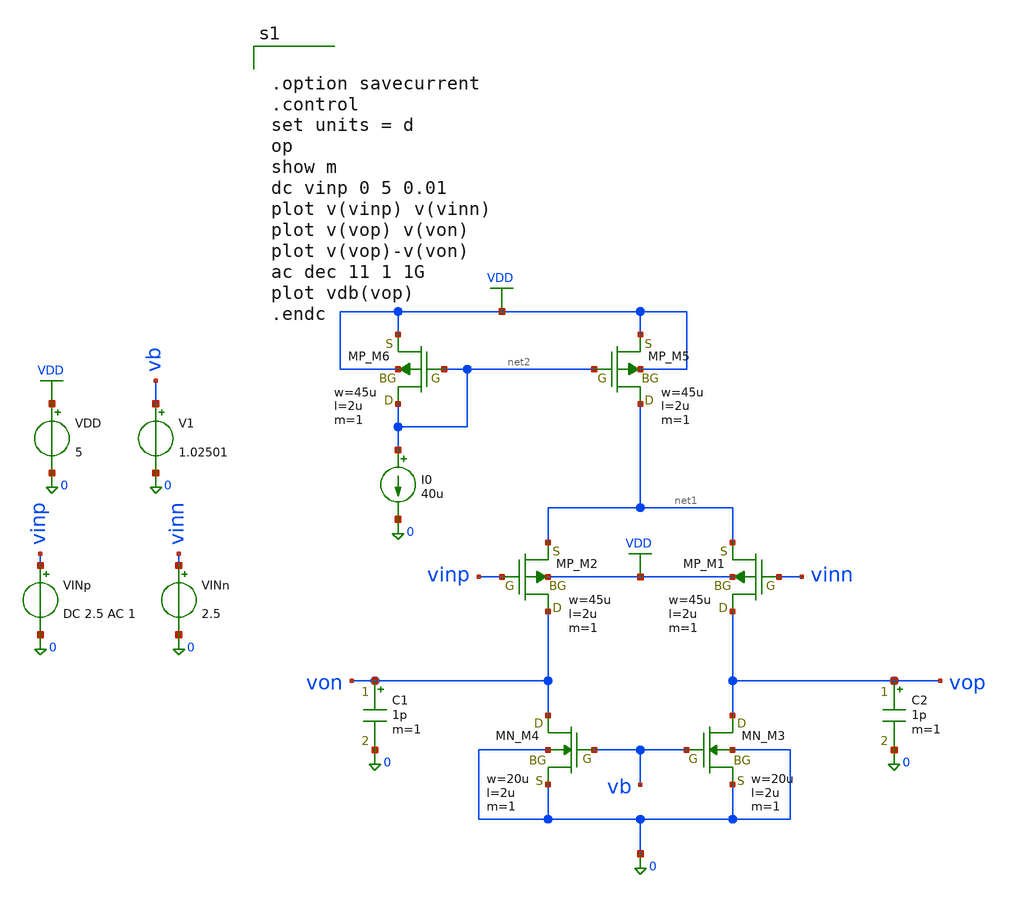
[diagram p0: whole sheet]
** sch_path: member_project/JJY_Receiver/Masahiro/jjy_recv/diff_amp/diff_amp.sch
**.subckt diff_amp
VDD VDD 0 5
VINp vinp 0 DC 2.5 AC 1
I0 net2 0 40u
C1 von 0 1p m=1
V1 vb 0 1.02501
XM1 vop vinn net1 VDD PMOS w=45u l=2u as=0 ad=0 ps=0 pd=0 nrd=0 nrs=0 m=1
XM2 von vinp net1 VDD PMOS w=45u l=2u as=0 ad=0 ps=0 pd=0 nrd=0 nrs=0 m=1
XM3 vop vb 0 0 NMOS w=20u l=2u as=0 ad=0 ps=0 pd=0 nrd=0 nrs=0 m=1
XM4 von vb 0 0 NMOS w=20u l=2u as=0 ad=0 ps=0 pd=0 nrd=0 nrs=0 m=1
XM5 net1 net2 VDD VDD PMOS w=45u l=2u as=0 ad=0 ps=0 pd=0 nrd=0 nrs=0 m=1
XM6 net2 net2 VDD VDD PMOS w=45u l=2u as=0 ad=0 ps=0 pd=0 nrd=0 nrs=0 m=1
C2 vop 0 1p m=1
VINn vinn 0 2.5
**** begin user architecture code
 .include $::LIB/ip62_models


.option savecurrent
.control
set units = d
op
show m
dc vinp 0 5 0.01
plot v(vinp) v(vinn)
plot v(vop) v(von)
plot v(vop)-v(von)
ac dec 11 1 1G
plot vdb(vop)
.endc


**** end user architecture code
**.ends
.GLOBAL VDD
.end
